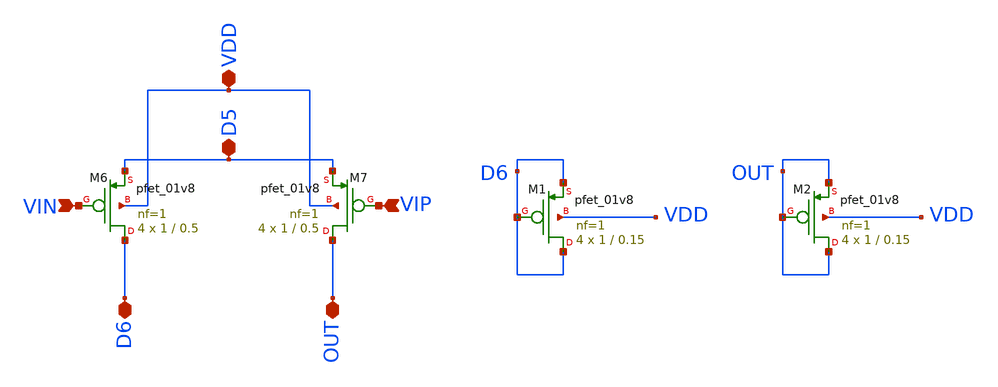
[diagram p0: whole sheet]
** sch_path: opamp/mag/pmoscs2.sch
**.subckt pmoscs2 VIN VIP D5 VDD D6 OUT
*.ipin VIN
*.ipin VIP
*.iopin D5
*.iopin VDD
*.iopin D6
*.iopin OUT
XM6 D6 VIN D5 VDD sky130_fd_pr__pfet_01v8 L=0.5 W=1 nf=1 ad='int((nf+1)/2) * W/nf * 0.29' as='int((nf+2)/2) * W/nf * 0.29'
+ pd='2*int((nf+1)/2) * (W/nf + 0.29)' ps='2*int((nf+2)/2) * (W/nf + 0.29)' nrd='0.29 / W' nrs='0.29 / W'
+ sa=0 sb=0 sd=0 mult=4 m=4
XM7 OUT VIP D5 VDD sky130_fd_pr__pfet_01v8 L=0.5 W=1 nf=1 ad='int((nf+1)/2) * W/nf * 0.29' as='int((nf+2)/2) * W/nf * 0.29'
+ pd='2*int((nf+1)/2) * (W/nf + 0.29)' ps='2*int((nf+2)/2) * (W/nf + 0.29)' nrd='0.29 / W' nrs='0.29 / W'
+ sa=0 sb=0 sd=0 mult=4 m=4
XM1 D6 D6 D6 VDD sky130_fd_pr__pfet_01v8 L=0.15 W=1 nf=1 ad='int((nf+1)/2) * W/nf * 0.29' as='int((nf+2)/2) * W/nf * 0.29'
+ pd='2*int((nf+1)/2) * (W/nf + 0.29)' ps='2*int((nf+2)/2) * (W/nf + 0.29)' nrd='0.29 / W' nrs='0.29 / W'
+ sa=0 sb=0 sd=0 mult=4 m=4
XM2 OUT OUT OUT VDD sky130_fd_pr__pfet_01v8 L=0.15 W=1 nf=1 ad='int((nf+1)/2) * W/nf * 0.29' as='int((nf+2)/2) * W/nf * 0.29'
+ pd='2*int((nf+1)/2) * (W/nf + 0.29)' ps='2*int((nf+2)/2) * (W/nf + 0.29)' nrd='0.29 / W' nrs='0.29 / W'
+ sa=0 sb=0 sd=0 mult=4 m=4
**.ends
.end
